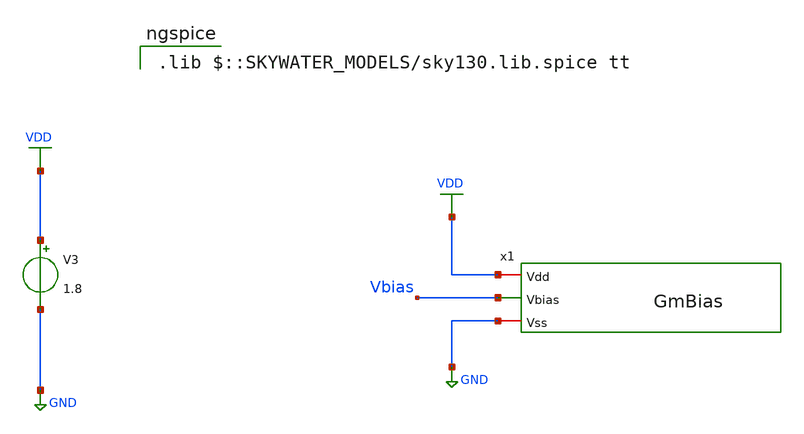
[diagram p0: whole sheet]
** sch_path: Circuits/Examples/OpAmp/GmBias_tb.sch
**.subckt GmBias_tb
x1 VDD Vbias GND GmBias
V3 VDD GND 1.8
**** begin user architecture code



* ngspice commands
.option savecurrents
.save all
.control
op
.endc



 .lib $::SKYWATER_MODELS/sky130.lib.spice tt

**** end user architecture code
**.ends

* expanding   symbol:  /home/jakob/Documents/RALF/Circuits/Examples/MillerOpAmpCMMFB/GmBias.sym # of
*+ pins=3
** sym_path: Circuits/Examples/OpAmp/GmBias.sym
** sch_path: Circuits/Examples/OpAmp/GmBias.sch
.subckt GmBias Vdd Vbias Vss
*.opin Vbias
*.iopin Vss
*.iopin Vdd
XM6 Vbias Vbias Vss Vss sky130_fd_pr__nfet_01v8 L=2 W=1 nf=1 ad='int((nf+1)/2) * W/nf * 0.29' as='int((nf+2)/2) * W/nf * 0.29'
+ pd='2*int((nf+1)/2) * (W/nf + 0.29)' ps='2*int((nf+2)/2) * (W/nf + 0.29)' nrd='0.29 / W' nrs='0.29 / W'
+ sa=0 sb=0 sd=0 mult=1 m=1
XM2 v1 v1 Vdd Vdd sky130_fd_pr__pfet_01v8 L=1 W=4 nf=2 ad='int((nf+1)/2) * W/nf * 0.29' as='int((nf+2)/2) * W/nf * 0.29'
+ pd='2*int((nf+1)/2) * (W/nf + 0.29)' ps='2*int((nf+2)/2) * (W/nf + 0.29)' nrd='0.29 / W' nrs='0.29 / W'
+ sa=0 sb=0 sd=0 mult=1 m=1
XM1 Vbias v1 Vdd Vdd sky130_fd_pr__pfet_01v8 L=1 W=4 nf=2 ad='int((nf+1)/2) * W/nf * 0.29' as='int((nf+2)/2) * W/nf * 0.29'
+ pd='2*int((nf+1)/2) * (W/nf + 0.29)' ps='2*int((nf+2)/2) * (W/nf + 0.29)' nrd='0.29 / W' nrs='0.29 / W'
+ sa=0 sb=0 sd=0 mult=1 m=1
XM3 v1 Vbias net1 Vss sky130_fd_pr__nfet_01v8 L=2 W=1 nf=1 ad='int((nf+1)/2) * W/nf * 0.29' as='int((nf+2)/2) * W/nf * 0.29'
+ pd='2*int((nf+1)/2) * (W/nf + 0.29)' ps='2*int((nf+2)/2) * (W/nf + 0.29)' nrd='0.29 / W' nrs='0.29 / W'
+ sa=0 sb=0 sd=0 mult=1 m=1
XR6 Vss net1 Vss sky130_fd_pr__res_xhigh_po_0p35 L=1 mult=1 m=1
XM4 v1 v1 Vbias Vss sky130_fd_pr__nfet_01v8 L=2 W=1 nf=1 ad='int((nf+1)/2) * W/nf * 0.29' as='int((nf+2)/2) * W/nf * 0.29'
+ pd='2*int((nf+1)/2) * (W/nf + 0.29)' ps='2*int((nf+2)/2) * (W/nf + 0.29)' nrd='0.29 / W' nrs='0.29 / W'
+ sa=0 sb=0 sd=0 mult=1 m=1
.ends

.GLOBAL GND
.GLOBAL VDD
.end
